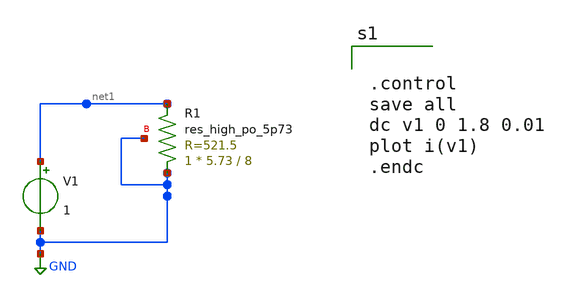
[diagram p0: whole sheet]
** sch_path: modules/testing_res/test/res_poly_corners.sch
**.subckt res_poly_corners
V1 net1 GND 1
XR1 GND net1 GND sky130_fd_pr__res_high_po_5p73 L=8 mult=1 m=1
**** begin user architecture code


.control
save all
dc v1 0 1.8 0.01
plot i(v1)
.endc



.lib $env(PDK_ROOT)/$env(PDK)/libs.tech/ngspice/sky130.lib.spice.tt.red tt
*.lib $env(PDK_ROOT)/$env(PDK)/libs.tech/combined/sky130.lib.spice tt

**** end user architecture code
**.ends
.GLOBAL GND
.end
